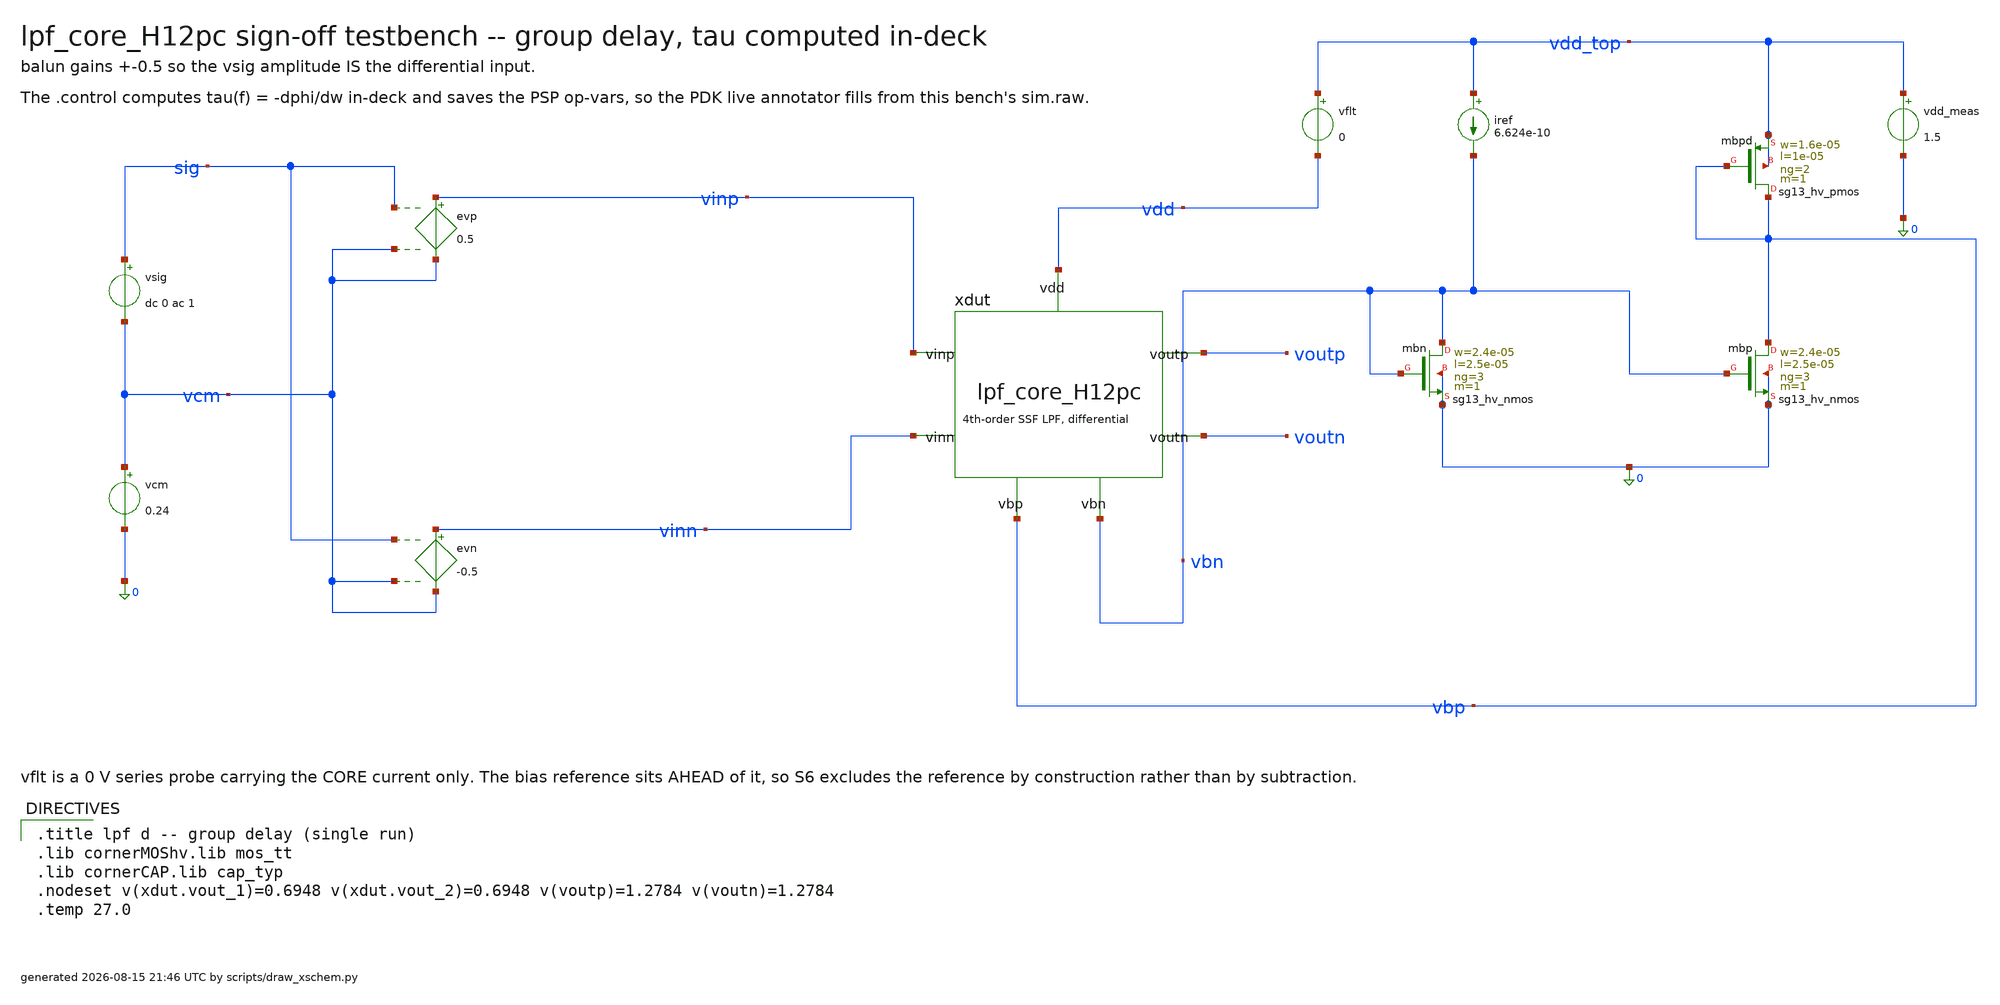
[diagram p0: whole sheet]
** sch_path: signoff/post-pvt/H12-pdk-cap/lpf_tb_H12pc_gd.sch
**.subckt lpf_tb_H12pc_gd
vsig sig vcm dc 0 ac 1
vcm vcm 0 0.24
evp vinp vcm sig vcm 0.5
evn vinn vcm sig vcm -0.5
xdut vinp vinn voutp voutn vbn vbp vdd lpf_core_H12pc
vflt vdd_top vdd 0
vdd_meas vdd_top 0 1.5
iref vdd_top vbn 6.624e-10
Xmbn vbn vbn 0 0 sg13_hv_nmos w=2.4e-05 l=2.5e-05 ng=3 m=1 mm_ok=1
Xmbp vbp vbn 0 0 sg13_hv_nmos w=2.4e-05 l=2.5e-05 ng=3 m=1 mm_ok=1
Xmbpd vbp vbp vdd_top vdd_top sg13_hv_pmos w=1.6e-05 l=1e-05 ng=2 m=1 mm_ok=1
**** begin user architecture code

.title lpf d -- group delay (single run)
.lib cornerMOShv.lib mos_tt
.lib cornerCAP.lib cap_typ
.nodeset v(xdut.vout_1)=0.6948 v(xdut.vout_2)=0.6948 v(voutp)=1.2784 v(voutn)=1.2784
.temp 27.0


.control
set filetype=binary
set appendwrite
save all @n.xdut.xm2.nsg13_hv_pmos[ids] @n.xdut.xm2.nsg13_hv_pmos[gm] @n.xdut.xm2.nsg13_hv_pmos[gds]
+ @n.xdut.xm2.nsg13_hv_pmos[gmb] @n.xdut.xm2.nsg13_hv_pmos[vgs] @n.xdut.xm2.nsg13_hv_pmos[vds] @n.xdut.xm2.nsg13_hv_pmos[vth]
+ @n.xdut.xm2.nsg13_hv_pmos[vdss] @n.xdut.xm2.nsg13_hv_pmos[cgg] @n.xdut.xm5.nsg13_hv_pmos[ids] @n.xdut.xm5.nsg13_hv_pmos[gm]
+ @n.xdut.xm5.nsg13_hv_pmos[gds] @n.xdut.xm5.nsg13_hv_pmos[gmb] @n.xdut.xm5.nsg13_hv_pmos[vgs] @n.xdut.xm5.nsg13_hv_pmos[vds]
+ @n.xdut.xm5.nsg13_hv_pmos[vth] @n.xdut.xm5.nsg13_hv_pmos[vdss] @n.xdut.xm5.nsg13_hv_pmos[cgg] @n.xdut.xm4.nsg13_hv_nmos[ids]
+ @n.xdut.xm4.nsg13_hv_nmos[gm] @n.xdut.xm4.nsg13_hv_nmos[gds] @n.xdut.xm4.nsg13_hv_nmos[gmb] @n.xdut.xm4.nsg13_hv_nmos[vgs]
+ @n.xdut.xm4.nsg13_hv_nmos[vds] @n.xdut.xm4.nsg13_hv_nmos[vth] @n.xdut.xm4.nsg13_hv_nmos[vdss] @n.xdut.xm4.nsg13_hv_nmos[cgg]
+ @n.xdut.xm8.nsg13_hv_nmos[ids] @n.xdut.xm8.nsg13_hv_nmos[gm] @n.xdut.xm8.nsg13_hv_nmos[gds] @n.xdut.xm8.nsg13_hv_nmos[gmb]
+ @n.xdut.xm8.nsg13_hv_nmos[vgs] @n.xdut.xm8.nsg13_hv_nmos[vds] @n.xdut.xm8.nsg13_hv_nmos[vth] @n.xdut.xm8.nsg13_hv_nmos[vdss]
+ @n.xdut.xm8.nsg13_hv_nmos[cgg] @n.xdut.xm9.nsg13_hv_nmos[ids] @n.xdut.xm9.nsg13_hv_nmos[gm] @n.xdut.xm9.nsg13_hv_nmos[gds]
+ @n.xdut.xm9.nsg13_hv_nmos[gmb] @n.xdut.xm9.nsg13_hv_nmos[vgs] @n.xdut.xm9.nsg13_hv_nmos[vds] @n.xdut.xm9.nsg13_hv_nmos[vth]
+ @n.xdut.xm9.nsg13_hv_nmos[vdss] @n.xdut.xm9.nsg13_hv_nmos[cgg] @n.xdut.xm10.nsg13_hv_nmos[ids] @n.xdut.xm10.nsg13_hv_nmos[gm]
+ @n.xdut.xm10.nsg13_hv_nmos[gds] @n.xdut.xm10.nsg13_hv_nmos[gmb] @n.xdut.xm10.nsg13_hv_nmos[vgs] @n.xdut.xm10.nsg13_hv_nmos[vds]
+ @n.xdut.xm10.nsg13_hv_nmos[vth] @n.xdut.xm10.nsg13_hv_nmos[vdss] @n.xdut.xm10.nsg13_hv_nmos[cgg] @n.xdut.xmst.nsg13_hv_pmos[ids]
+ @n.xdut.xmst.nsg13_hv_pmos[gm] @n.xdut.xmst.nsg13_hv_pmos[gds] @n.xdut.xmst.nsg13_hv_pmos[gmb] @n.xdut.xmst.nsg13_hv_pmos[vgs]
+ @n.xdut.xmst.nsg13_hv_pmos[vds] @n.xdut.xmst.nsg13_hv_pmos[vth] @n.xdut.xmst.nsg13_hv_pmos[vdss] @n.xdut.xmst.nsg13_hv_pmos[cgg]
+ @n.xdut.xmstn.nsg13_hv_pmos[ids] @n.xdut.xmstn.nsg13_hv_pmos[gm] @n.xdut.xmstn.nsg13_hv_pmos[gds] @n.xdut.xmstn.nsg13_hv_pmos[gmb]
+ @n.xdut.xmstn.nsg13_hv_pmos[vgs] @n.xdut.xmstn.nsg13_hv_pmos[vds] @n.xdut.xmstn.nsg13_hv_pmos[vth] @n.xdut.xmstn.nsg13_hv_pmos[vdss]
+ @n.xdut.xmstn.nsg13_hv_pmos[cgg] @n.xdut.xm0.nsg13_hv_pmos[ids] @n.xdut.xm0.nsg13_hv_pmos[gm] @n.xdut.xm0.nsg13_hv_pmos[gds]
+ @n.xdut.xm0.nsg13_hv_pmos[gmb] @n.xdut.xm0.nsg13_hv_pmos[vgs] @n.xdut.xm0.nsg13_hv_pmos[vds] @n.xdut.xm0.nsg13_hv_pmos[vth]
+ @n.xdut.xm0.nsg13_hv_pmos[vdss] @n.xdut.xm0.nsg13_hv_pmos[cgg] @n.xdut.xm1.nsg13_hv_pmos[ids] @n.xdut.xm1.nsg13_hv_pmos[gm]
+ @n.xdut.xm1.nsg13_hv_pmos[gds] @n.xdut.xm1.nsg13_hv_pmos[gmb] @n.xdut.xm1.nsg13_hv_pmos[vgs] @n.xdut.xm1.nsg13_hv_pmos[vds]
+ @n.xdut.xm1.nsg13_hv_pmos[vth] @n.xdut.xm1.nsg13_hv_pmos[vdss] @n.xdut.xm1.nsg13_hv_pmos[cgg] @n.xdut.xm14.nsg13_hv_pmos[ids]
+ @n.xdut.xm14.nsg13_hv_pmos[gm] @n.xdut.xm14.nsg13_hv_pmos[gds] @n.xdut.xm14.nsg13_hv_pmos[gmb] @n.xdut.xm14.nsg13_hv_pmos[vgs]
+ @n.xdut.xm14.nsg13_hv_pmos[vds] @n.xdut.xm14.nsg13_hv_pmos[vth] @n.xdut.xm14.nsg13_hv_pmos[vdss] @n.xdut.xm14.nsg13_hv_pmos[cgg]
+ @n.xdut.xm15.nsg13_hv_pmos[ids] @n.xdut.xm15.nsg13_hv_pmos[gm] @n.xdut.xm15.nsg13_hv_pmos[gds] @n.xdut.xm15.nsg13_hv_pmos[gmb]
+ @n.xdut.xm15.nsg13_hv_pmos[vgs] @n.xdut.xm15.nsg13_hv_pmos[vds] @n.xdut.xm15.nsg13_hv_pmos[vth] @n.xdut.xm15.nsg13_hv_pmos[vdss]
+ @n.xdut.xm15.nsg13_hv_pmos[cgg] @n.xdut.xr1.nsg13_hv_pmos[ids] @n.xdut.xr1.nsg13_hv_pmos[gm] @n.xdut.xr1.nsg13_hv_pmos[gds]
+ @n.xdut.xr1.nsg13_hv_pmos[gmb] @n.xdut.xr1.nsg13_hv_pmos[vgs] @n.xdut.xr1.nsg13_hv_pmos[vds] @n.xdut.xr1.nsg13_hv_pmos[vth]
+ @n.xdut.xr1.nsg13_hv_pmos[vdss] @n.xdut.xr1.nsg13_hv_pmos[cgg] @n.xdut.xr1.nsg13_hv_pmos[ids] @n.xdut.xr1.nsg13_hv_pmos[gm]
+ @n.xdut.xr1.nsg13_hv_pmos[gds] @n.xdut.xr1.nsg13_hv_pmos[gmb] @n.xdut.xr1.nsg13_hv_pmos[vgs] @n.xdut.xr1.nsg13_hv_pmos[vds]
+ @n.xdut.xr1.nsg13_hv_pmos[vth] @n.xdut.xr1.nsg13_hv_pmos[vdss] @n.xdut.xr1.nsg13_hv_pmos[cgg] @n.xdut.xr2.nsg13_hv_pmos[ids]
+ @n.xdut.xr2.nsg13_hv_pmos[gm] @n.xdut.xr2.nsg13_hv_pmos[gds] @n.xdut.xr2.nsg13_hv_pmos[gmb] @n.xdut.xr2.nsg13_hv_pmos[vgs]
+ @n.xdut.xr2.nsg13_hv_pmos[vds] @n.xdut.xr2.nsg13_hv_pmos[vth] @n.xdut.xr2.nsg13_hv_pmos[vdss] @n.xdut.xr2.nsg13_hv_pmos[cgg]
+ @n.xdut.xr2.nsg13_hv_pmos[ids] @n.xdut.xr2.nsg13_hv_pmos[gm] @n.xdut.xr2.nsg13_hv_pmos[gds] @n.xdut.xr2.nsg13_hv_pmos[gmb]
+ @n.xdut.xr2.nsg13_hv_pmos[vgs] @n.xdut.xr2.nsg13_hv_pmos[vds] @n.xdut.xr2.nsg13_hv_pmos[vth] @n.xdut.xr2.nsg13_hv_pmos[vdss]
+ @n.xdut.xr2.nsg13_hv_pmos[cgg] @n.xdut.xr3.nsg13_hv_nmos[ids] @n.xdut.xr3.nsg13_hv_nmos[gm] @n.xdut.xr3.nsg13_hv_nmos[gds]
+ @n.xdut.xr3.nsg13_hv_nmos[gmb] @n.xdut.xr3.nsg13_hv_nmos[vgs] @n.xdut.xr3.nsg13_hv_nmos[vds] @n.xdut.xr3.nsg13_hv_nmos[vth]
+ @n.xdut.xr3.nsg13_hv_nmos[vdss] @n.xdut.xr3.nsg13_hv_nmos[cgg] @n.xdut.xr3.nsg13_hv_nmos[ids] @n.xdut.xr3.nsg13_hv_nmos[gm]
+ @n.xdut.xr3.nsg13_hv_nmos[gds] @n.xdut.xr3.nsg13_hv_nmos[gmb] @n.xdut.xr3.nsg13_hv_nmos[vgs] @n.xdut.xr3.nsg13_hv_nmos[vds]
+ @n.xdut.xr3.nsg13_hv_nmos[vth] @n.xdut.xr3.nsg13_hv_nmos[vdss] @n.xdut.xr3.nsg13_hv_nmos[cgg]
op
write sim.raw
ac dec 50 0.1 1000
let hdiff = v(voutp) - v(voutn)
let hdb = db(mag(hdiff))
let dc_db = hdb[0]
let ph = cph(hdiff)
let gd = -deriv(ph) / (2 * pi)
let gd_dc_ms = gd[0] * 1e3
let gd_max_ms = vecmax(gd) * 1e3
let hrel = hdb - dc_db
meas ac fc_hz when hrel = -3 fall = 1
print dc_db gd_dc_ms gd_max_ms
write sim.raw hdiff ph gd frequency
.endc

**** end user architecture code
**.ends

* expanding   symbol:  lpf_core_H12pc.sym # of pins=7
** sym_path: signoff/post-pvt/H12-pdk-cap/lpf_core_H12pc.sym
** sch_path: signoff/post-pvt/H12-pdk-cap/lpf_core_H12pc.sch
.subckt lpf_core_H12pc vinp vinn voutp voutn vbn vbp vdd
*.ipin vinp
*.ipin vinn
*.opin voutp
*.opin voutn
*.ipin vdd
*.ipin vbn
*.ipin vbp
Xm2 net2 vinp vout_1 vout_1 sg13_hv_pmos w=1.6e-05 l=1e-05 ng=2 m=1 mm_ok=1
Xm5 net3 vinn vout_2 vout_2 sg13_hv_pmos w=1.6e-05 l=1e-05 ng=2 m=1 mm_ok=1
Xm4 vout_1 net2 0 0 sg13_hv_nmos w=1.5e-06 l=4.5e-05 ng=1 m=1 mm_ok=1
Xm8 vout_2 net3 0 0 sg13_hv_nmos w=1.5e-06 l=4.5e-05 ng=1 m=1 mm_ok=1
Xm9 net2 vbn 0 0 sg13_hv_nmos w=2.4e-05 l=2.5e-05 ng=3 m=1 mm_ok=1
Xm10 net3 vbn 0 0 sg13_hv_nmos w=2.4e-05 l=2.5e-05 ng=3 m=1 mm_ok=1
Xmst vout_1 vbr net4 net4 sg13_hv_pmos w=5e-06 l=3.3e-05 ng=1 m=1 mm_ok=1
Xmstn vout_2 vbr net1 net1 sg13_hv_pmos w=5e-06 l=3.3e-05 ng=1 m=1 mm_ok=1
Xm0 net4 vout_1 voutp voutp sg13_hv_pmos w=4e-06 l=1.5e-05 ng=1 m=1 mm_ok=1
Xm1 net1 vout_2 voutn voutn sg13_hv_pmos w=4e-06 l=1.5e-05 ng=1 m=1 mm_ok=1
Xm14 voutp net4 vdd vdd sg13_hv_pmos w=1.2e-05 l=3.1e-05 ng=2 m=1 mm_ok=1
Xm15 voutn net1 vdd vdd sg13_hv_pmos w=1.2e-05 l=3.1e-05 ng=2 m=1 mm_ok=1
Xr1 rep_x rep_x vdd vdd sg13_hv_pmos w=1.2e-05 l=3.1e-05 ng=2 m=1 mm_ok=1
Xr2 vbr vbr rep_x rep_x sg13_hv_pmos w=5e-06 l=3.3e-05 ng=1 m=1 mm_ok=1
Xr3 vbr vbn 0 0 sg13_hv_nmos w=2.4e-05 l=2.5e-05 ng=3 m=4 mm_ok=1
Xc13 net2 vout_1 cap_cmim w=40.53u l=40.53u m=2 mm_ok=1
Xc17 net3 vout_2 cap_cmim w=40.53u l=40.53u m=2 mm_ok=1
Xc19 vout_2 vout_1 cap_cmim w=49.42u l=49.42u m=8 mm_ok=1
Xc1 voutp net4 cap_cmim w=49.91u l=49.91u m=16 mm_ok=1
Xc10 voutn net1 cap_cmim w=49.91u l=49.91u m=16 mm_ok=1
Xc12 voutn voutp cap_cmim w=48.45u l=48.45u m=7 mm_ok=1
.ends

.end
